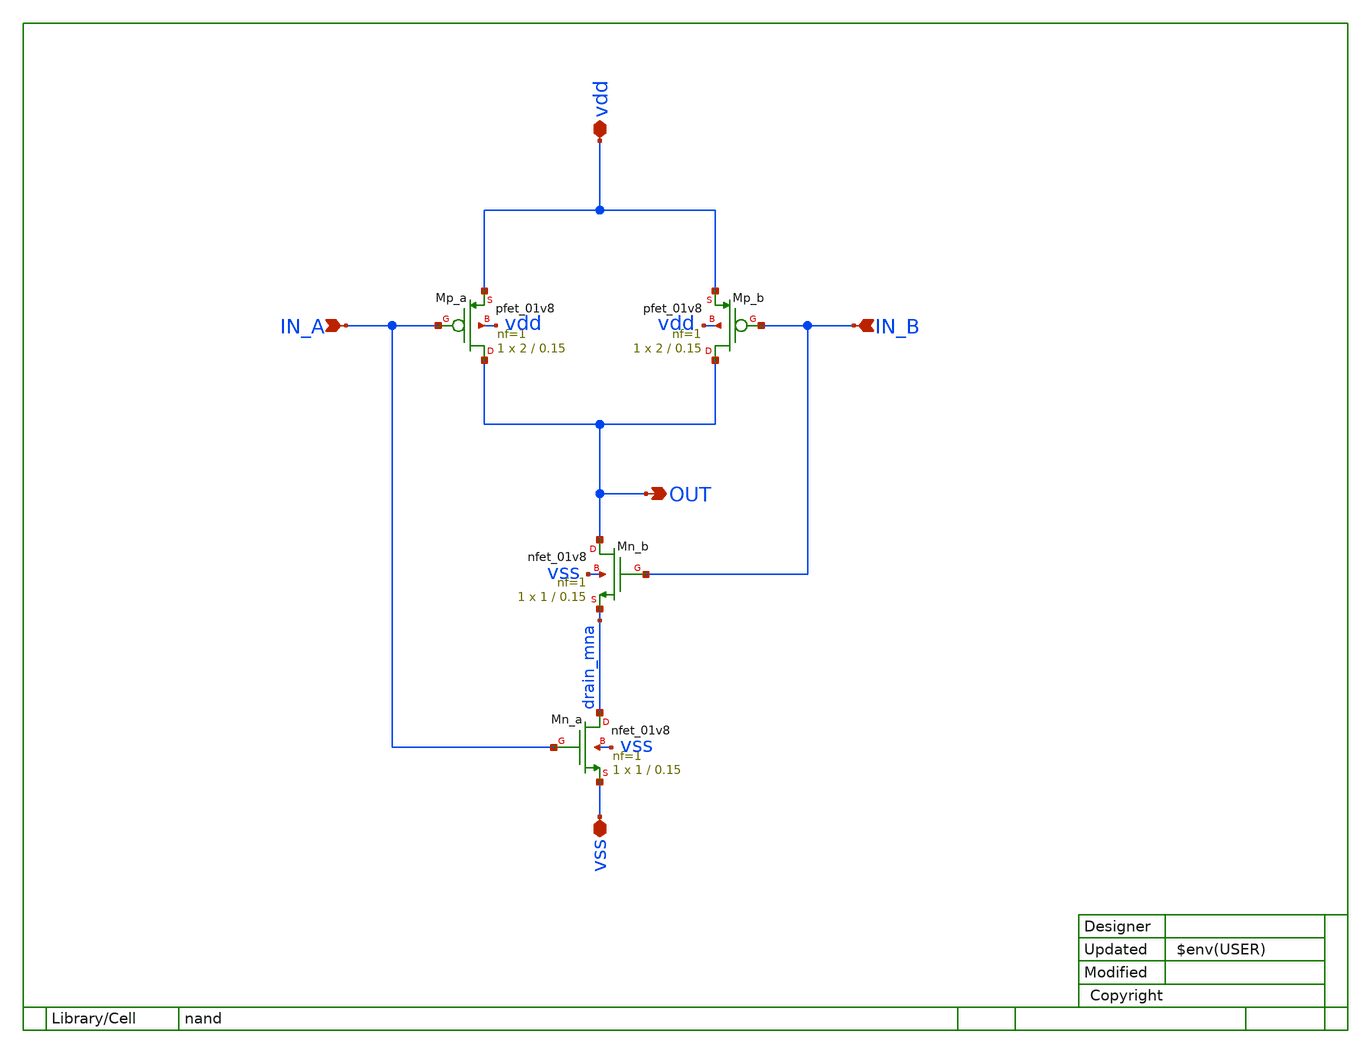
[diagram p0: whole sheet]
** sch_path: xsch/ip/logic/nand/nand.sch
**.subckt nand IN_A OUT vdd IN_B vss
*.ipin IN_A
*.opin OUT
*.iopin vdd
*.ipin IN_B
*.iopin vss
XMn_a drain_mna IN_A vss vss sky130_fd_pr__nfet_01v8 L=0.15 W=1 nf=1 ad='int((1 + 1)/2) * 1 / 1 * 0.29'
+ as='int((1 + 2)/2) * 1 / 1 * 0.29' pd='2*int((1 + 1)/2) * (1 / 1 + 0.29)' ps='2*int((1 + 2)/2) * (1 / 1 + 0.29)'
+ nrd='0.29 / 1 ' nrs='0.29 / 1 ' sa=0 sb=0 sd=0 mult=1 m=1
XMp_a OUT IN_A vdd vdd sky130_fd_pr__pfet_01v8 L=0.15 W=2 nf=1 ad='int((nf+1)/2) * W/nf * 0.29' as='int((nf+2)/2) * W/nf * 0.29'
+ pd='2*int((nf+1)/2) * (W/nf + 0.29)' ps='2*int((nf+2)/2) * (W/nf + 0.29)' nrd='0.29 / W' nrs='0.29 / W'
+ sa=0 sb=0 sd=0 mult=1 m=1
XMp_b OUT IN_B vdd vdd sky130_fd_pr__pfet_01v8 L=0.15 W=2 nf=1 ad='int((nf+1)/2) * W/nf * 0.29' as='int((nf+2)/2) * W/nf * 0.29'
+ pd='2*int((nf+1)/2) * (W/nf + 0.29)' ps='2*int((nf+2)/2) * (W/nf + 0.29)' nrd='0.29 / W' nrs='0.29 / W'
+ sa=0 sb=0 sd=0 mult=1 m=1
XMn_b OUT IN_B drain_mna vss sky130_fd_pr__nfet_01v8 L=0.15 W=1 nf=1 ad='int((1 + 1)/2) * 1 / 1 * 0.29'
+ as='int((1 + 2)/2) * 1 / 1 * 0.29' pd='2*int((1 + 1)/2) * (1 / 1 + 0.29)' ps='2*int((1 + 2)/2) * (1 / 1 + 0.29)'
+ nrd='0.29 / 1 ' nrs='0.29 / 1 ' sa=0 sb=0 sd=0 mult=1 m=1
**.ends
.end
